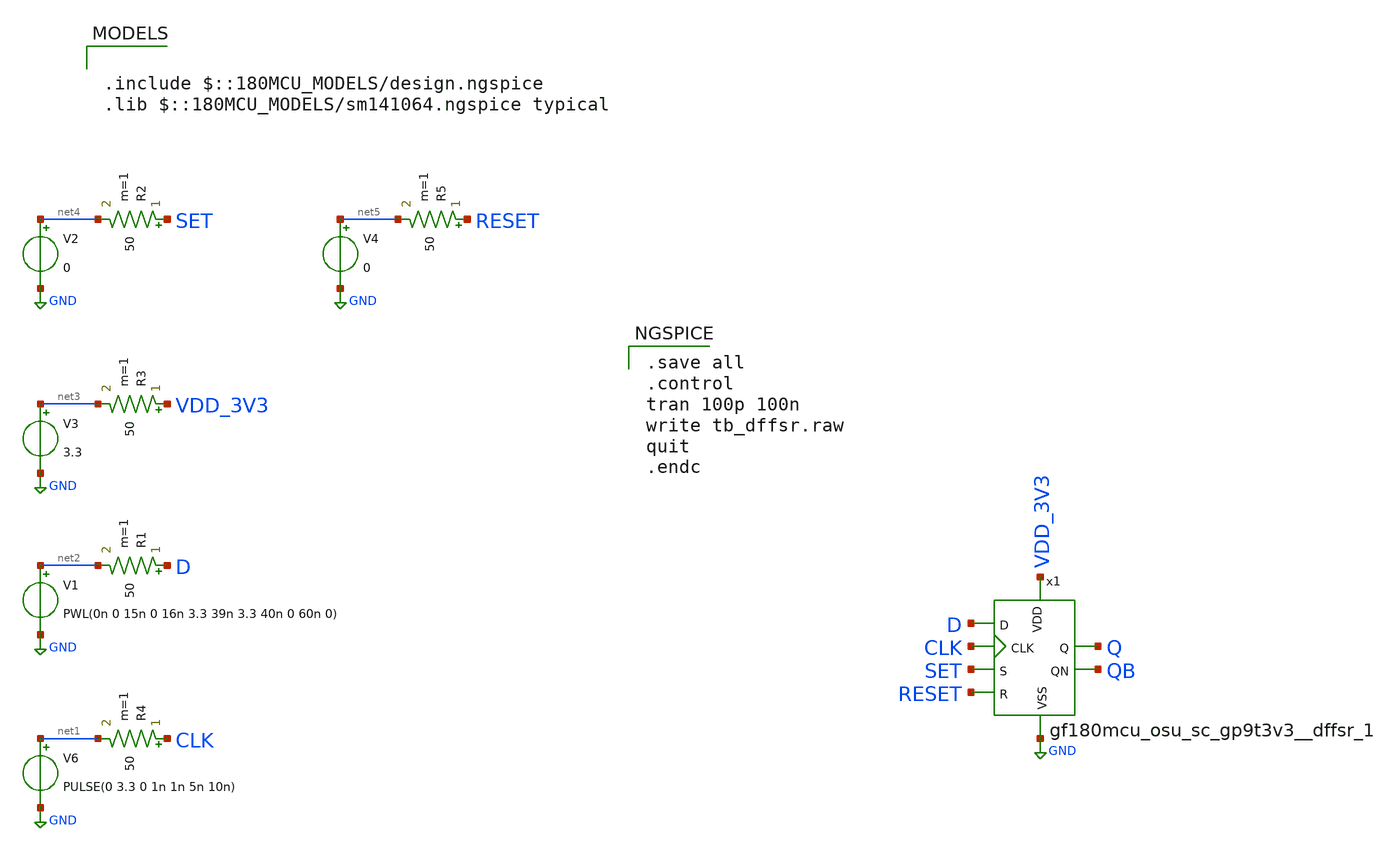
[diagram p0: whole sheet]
** sch_path: designs/libs/adc_singlecycle/tb_dffsr.sch
**.subckt tb_dffsr
V6 net1 GND PULSE(0 3.3 0 1n 1n 5n 10n)
R4 CLK net1 50 m=1
V1 net2 GND PWL(0n 0 15n 0 16n 3.3 39n 3.3 40n 0 60n 0)
R1 D net2 50 m=1
V3 net3 GND 3.3
R3 VDD_3V3 net3 50 m=1
V2 net4 GND 0
R2 SET net4 50 m=1
V4 net5 GND 0
R5 RESET net5 50 m=1
x1 RESET CLK D Q SET VDD_3V3 QB GND gf180mcu_osu_sc_gp9t3v3__dffsr_1
**** begin user architecture code

.include $::180MCU_MODELS/design.ngspice
.lib $::180MCU_MODELS/sm141064.ngspice typical


.save all
.control
tran 100p 100n
write tb_dffsr.raw
quit
.endc

**** end user architecture code
**.ends
.GLOBAL GND
.end
